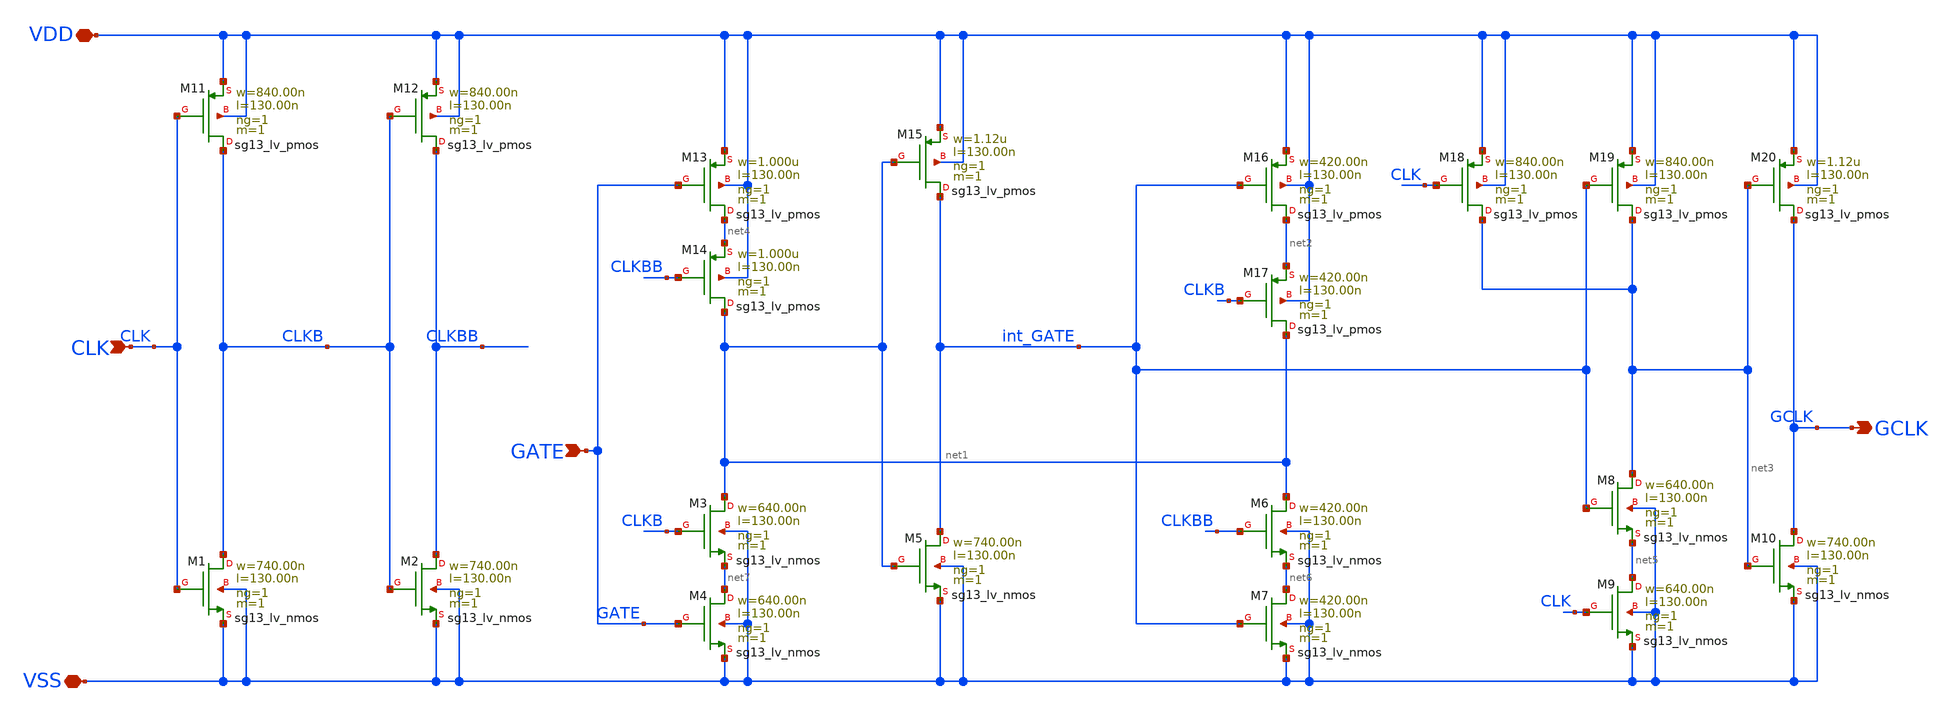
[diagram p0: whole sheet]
** sch_path: ihp-sg13g2/libs.tech/xschem/sg13g2_stdcells/sg13g2_lgcp_1.sch
**.subckt sg13g2_lgcp_1 GCLK GATE CLK VDD VSS
*.opin GCLK
*.ipin GATE
*.ipin CLK
*.iopin VDD
*.iopin VSS
XM1 CLKB CLK VSS VSS sg13_lv_nmos w=740.00n l=130.00n ng=1 m=1 mm_ok=1
XM2 CLKBB CLKB VSS VSS sg13_lv_nmos w=740.00n l=130.00n ng=1 m=1 mm_ok=1
XM3 net1 CLKB net7 VSS sg13_lv_nmos w=640.00n l=130.00n ng=1 m=1 mm_ok=1
XM4 net7 GATE VSS VSS sg13_lv_nmos w=640.00n l=130.00n ng=1 m=1 mm_ok=1
XM5 int_GATE net1 VSS VSS sg13_lv_nmos w=740.00n l=130.00n ng=1 m=1 mm_ok=1
XM6 net1 CLKBB net6 VSS sg13_lv_nmos w=420.00n l=130.00n ng=1 m=1 mm_ok=1
XM7 net6 int_GATE VSS VSS sg13_lv_nmos w=420.00n l=130.00n ng=1 m=1 mm_ok=1
XM8 net3 int_GATE net5 VSS sg13_lv_nmos w=640.00n l=130.00n ng=1 m=1 mm_ok=1
XM9 net5 CLK VSS VSS sg13_lv_nmos w=640.00n l=130.00n ng=1 m=1 mm_ok=1
XM10 GCLK net3 VSS VSS sg13_lv_nmos w=740.00n l=130.00n ng=1 m=1 mm_ok=1
XM11 CLKB CLK VDD VDD sg13_lv_pmos w=840.00n l=130.00n ng=1 m=1 mm_ok=1
XM12 CLKBB CLKB VDD VDD sg13_lv_pmos w=840.00n l=130.00n ng=1 m=1 mm_ok=1
XM13 net4 GATE VDD VDD sg13_lv_pmos w=1.000u l=130.00n ng=1 m=1 mm_ok=1
XM14 net1 CLKBB net4 VDD sg13_lv_pmos w=1.000u l=130.00n ng=1 m=1 mm_ok=1
XM15 int_GATE net1 VDD VDD sg13_lv_pmos w=1.12u l=130.00n ng=1 m=1 mm_ok=1
XM16 net2 int_GATE VDD VDD sg13_lv_pmos w=420.00n l=130.00n ng=1 m=1 mm_ok=1
XM17 net1 CLKB net2 VDD sg13_lv_pmos w=420.00n l=130.00n ng=1 m=1 mm_ok=1
XM18 net3 CLK VDD VDD sg13_lv_pmos w=840.00n l=130.00n ng=1 m=1 mm_ok=1
XM19 net3 int_GATE VDD VDD sg13_lv_pmos w=840.00n l=130.00n ng=1 m=1 mm_ok=1
XM20 GCLK net3 VDD VDD sg13_lv_pmos w=1.12u l=130.00n ng=1 m=1 mm_ok=1
**.ends
.end
